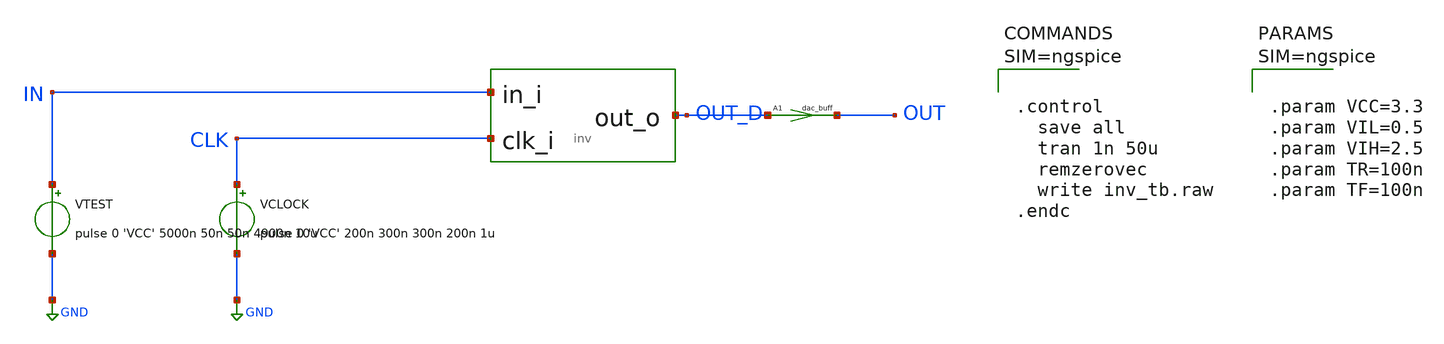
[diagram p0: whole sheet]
** sch_path: inv_tb.sch
**.subckt inv_tb
ADUT [ CLK IN ] [ OUT_D ] dut
VCLOCK CLK GND pulse 0 'VCC' 200n 300n 300n 200n 1u
VTEST IN GND pulse 0 'VCC' 5000n 50n 50n 4900n 10u
A1 [ OUT_D ] [ OUT ] dac_buff
**** begin user architecture code



.control
  save all
  tran 1n 50u
  remzerovec
  write inv_tb.raw
.endc






.param VCC=3.3
.param VIL=0.5
.param VIH=2.5
.param TR=100n
.param TF=100n



**** end user architecture code
**.ends
.GLOBAL GND
**** begin user architecture code
.model dut d_cosim simulation="ivlng" sim_args=["inv"]
.model dac_buff dac_bridge t_rise='TR' t_fall='TF'  out_low=0 out_high='VCC'
**** end user architecture code
.end
